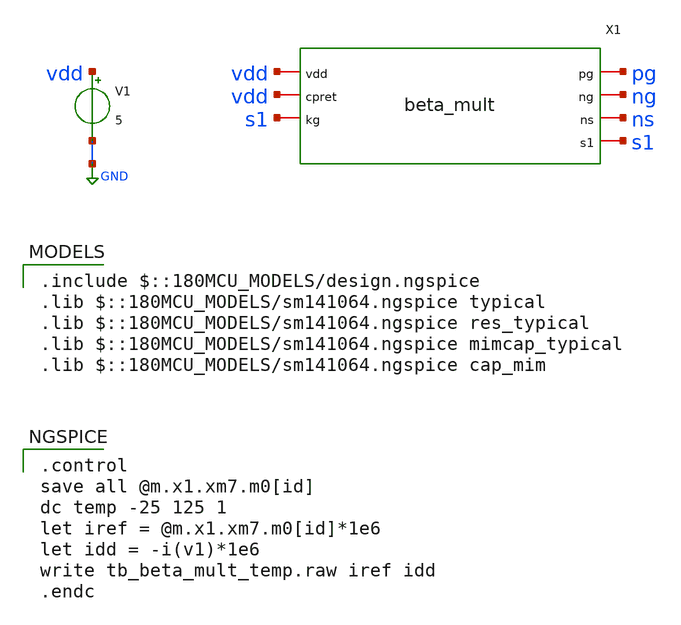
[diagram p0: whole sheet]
** sch_path: Schematics #2/sims/tb/tb_beta_mult_temp.sch
**.subckt tb_beta_mult_temp
V1 vdd GND 5
X1 vdd pg ng ns vdd s1 s1 beta_mult
**** begin user architecture code
 .include $::180MCU_MODELS/design.ngspice
.lib $::180MCU_MODELS/sm141064.ngspice typical
.lib $::180MCU_MODELS/sm141064.ngspice res_typical
.lib $::180MCU_MODELS/sm141064.ngspice mimcap_typical
.lib $::180MCU_MODELS/sm141064.ngspice cap_mim

.control
save all @m.x1.xm7.m0[id]
dc temp -25 125 1
let iref = @m.x1.xm7.m0[id]*1e6
let idd = -i(v1)*1e6
write tb_beta_mult_temp.raw iref idd
.endc

**** end user architecture code
**.ends
.GLOBAL GND
.end
